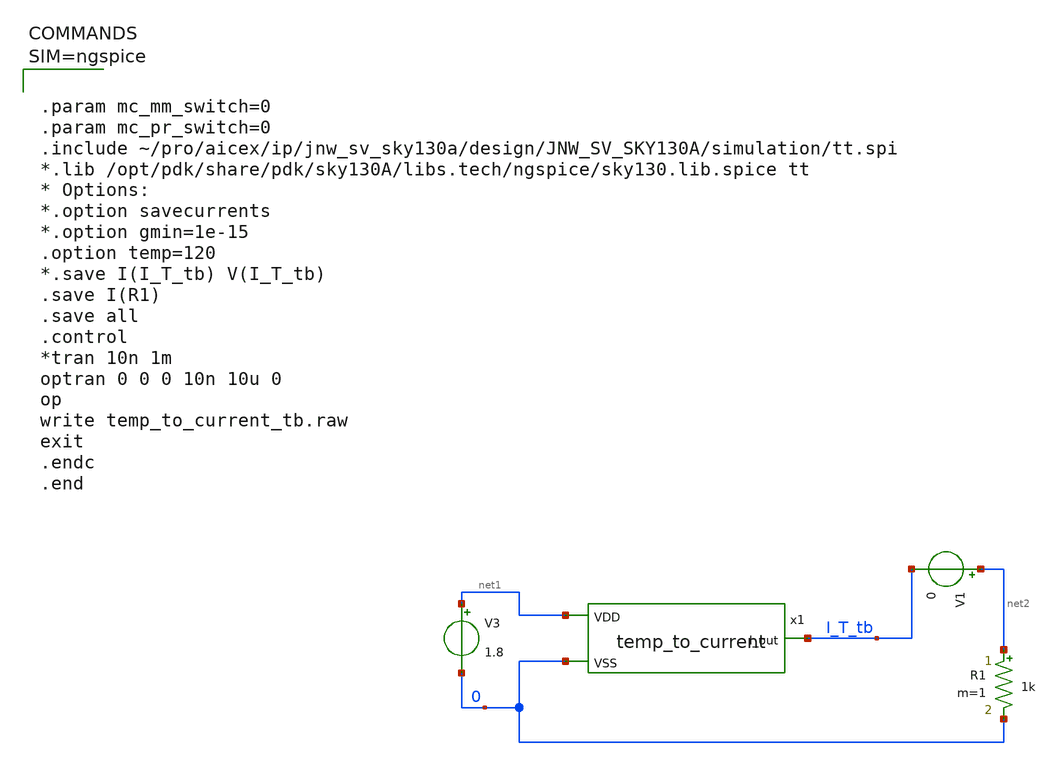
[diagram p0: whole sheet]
** sch_path: design/JNW_GR07_SKY130A/temp_to_current_tb_2.sch
**.subckt temp_to_current_tb_2
x1 net1 I_T_tb 0 temp_to_current
V3 net1 0 1.8
R1 net2 0 1k m=1
V1 net2 I_T_tb 0
**** begin user architecture code



.param mc_mm_switch=0
.param mc_pr_switch=0
.include ~/pro/aicex/ip/jnw_sv_sky130a/design/JNW_SV_SKY130A/simulation/tt.spi
*.lib /opt/pdk/share/pdk/sky130A/libs.tech/ngspice/sky130.lib.spice tt
* Options:
*.option savecurrents
*.option gmin=1e-15
.option temp=120
*.save I(I_T_tb) V(I_T_tb)
.save I(R1)
.save all
.control
*tran 10n 1m
optran 0 0 0 10n 10u 0
op
write temp_to_current_tb.raw
exit
.endc
.end



**** end user architecture code
**.ends
.end
